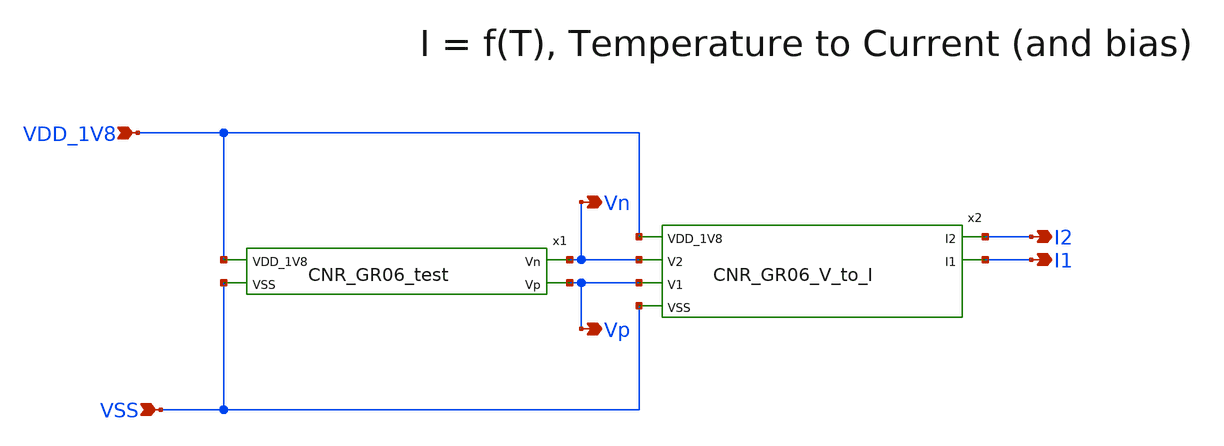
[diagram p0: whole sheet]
** sch_path: design/CNR_GR06_SKY130NM/CNR_GR06.sch
**.subckt CNR_GR06 VDD_1V8 VSS I2 I1 Vn Vp
*.ipin VDD_1V8
*.ipin VSS
*.opin I2
*.opin I1
*.opin Vn
*.opin Vp
x1 VDD_1V8 Vn Vp VSS CNR_GR06_test
x2 VDD_1V8 I2 I1 Vn Vp VSS CNR_GR06_V_to_I
**.ends
.end
